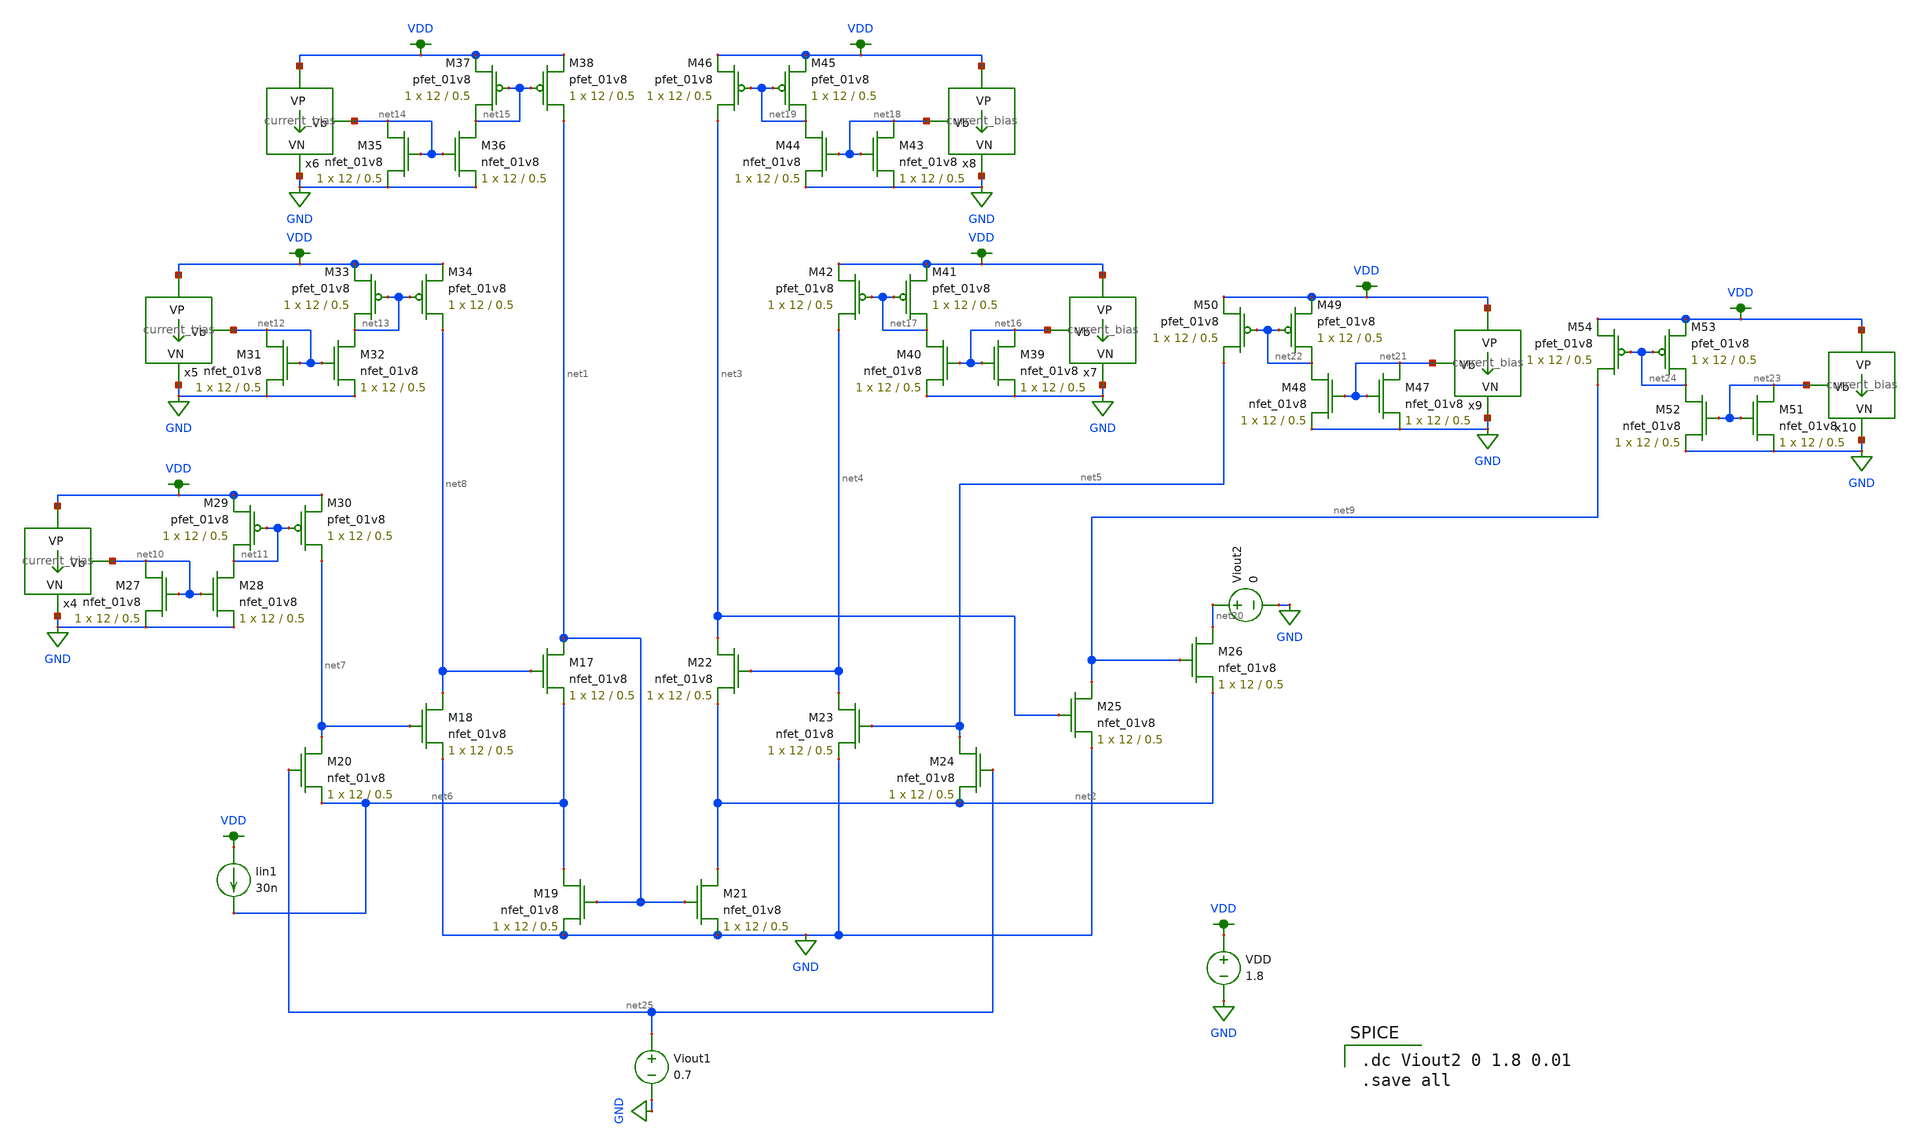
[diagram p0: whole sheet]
** sch_path: schematics/current mirrors/FVF_current_mirror_4.sch
**.subckt FVF_current_mirror_4
VDD VDD GND 1.8
XM19 net6 net1 GND GND sky130_fd_pr__nfet_01v8 L=0.5 W=12 nf=1 ad='int((nf+1)/2) * W/nf * 0.29' as='int((nf+2)/2) * W/nf * 0.29'
+ pd='2*int((nf+1)/2) * (W/nf + 0.29)' ps='2*int((nf+2)/2) * (W/nf + 0.29)' nrd='0.29 / W' nrs='0.29 / W'
+ sa=0 sb=0 sd=0 mult=1 m=1
XM21 net2 net1 GND GND sky130_fd_pr__nfet_01v8 L=0.5 W=12 nf=1 ad='int((nf+1)/2) * W/nf * 0.29' as='int((nf+2)/2) * W/nf * 0.29'
+ pd='2*int((nf+1)/2) * (W/nf + 0.29)' ps='2*int((nf+2)/2) * (W/nf + 0.29)' nrd='0.29 / W' nrs='0.29 / W'
+ sa=0 sb=0 sd=0 mult=1 m=1
XM22 net3 net4 net2 GND sky130_fd_pr__nfet_01v8 L=0.5 W=12 nf=1 ad='int((nf+1)/2) * W/nf * 0.29' as='int((nf+2)/2) * W/nf * 0.29'
+ pd='2*int((nf+1)/2) * (W/nf + 0.29)' ps='2*int((nf+2)/2) * (W/nf + 0.29)' nrd='0.29 / W' nrs='0.29 / W'
+ sa=0 sb=0 sd=0 mult=1 m=1
XM23 net4 net5 GND GND sky130_fd_pr__nfet_01v8 L=0.5 W=12 nf=1 ad='int((nf+1)/2) * W/nf * 0.29' as='int((nf+2)/2) * W/nf * 0.29'
+ pd='2*int((nf+1)/2) * (W/nf + 0.29)' ps='2*int((nf+2)/2) * (W/nf + 0.29)' nrd='0.29 / W' nrs='0.29 / W'
+ sa=0 sb=0 sd=0 mult=1 m=1
XM24 net5 net25 net2 GND sky130_fd_pr__nfet_01v8 L=0.5 W=12 nf=1 ad='int((nf+1)/2) * W/nf * 0.29' as='int((nf+2)/2) * W/nf * 0.29'
+ pd='2*int((nf+1)/2) * (W/nf + 0.29)' ps='2*int((nf+2)/2) * (W/nf + 0.29)' nrd='0.29 / W' nrs='0.29 / W'
+ sa=0 sb=0 sd=0 mult=1 m=1
XM17 net1 net8 net6 GND sky130_fd_pr__nfet_01v8 L=0.5 W=12 nf=1 ad='int((nf+1)/2) * W/nf * 0.29' as='int((nf+2)/2) * W/nf * 0.29'
+ pd='2*int((nf+1)/2) * (W/nf + 0.29)' ps='2*int((nf+2)/2) * (W/nf + 0.29)' nrd='0.29 / W' nrs='0.29 / W'
+ sa=0 sb=0 sd=0 mult=1 m=1
XM18 net8 net7 GND GND sky130_fd_pr__nfet_01v8 L=0.5 W=12 nf=1 ad='int((nf+1)/2) * W/nf * 0.29' as='int((nf+2)/2) * W/nf * 0.29'
+ pd='2*int((nf+1)/2) * (W/nf + 0.29)' ps='2*int((nf+2)/2) * (W/nf + 0.29)' nrd='0.29 / W' nrs='0.29 / W'
+ sa=0 sb=0 sd=0 mult=1 m=1
XM20 net7 net25 net6 GND sky130_fd_pr__nfet_01v8 L=0.5 W=12 nf=1 ad='int((nf+1)/2) * W/nf * 0.29' as='int((nf+2)/2) * W/nf * 0.29'
+ pd='2*int((nf+1)/2) * (W/nf + 0.29)' ps='2*int((nf+2)/2) * (W/nf + 0.29)' nrd='0.29 / W' nrs='0.29 / W'
+ sa=0 sb=0 sd=0 mult=1 m=1
XM25 net9 net3 GND GND sky130_fd_pr__nfet_01v8 L=0.5 W=12 nf=1 ad='int((nf+1)/2) * W/nf * 0.29' as='int((nf+2)/2) * W/nf * 0.29'
+ pd='2*int((nf+1)/2) * (W/nf + 0.29)' ps='2*int((nf+2)/2) * (W/nf + 0.29)' nrd='0.29 / W' nrs='0.29 / W'
+ sa=0 sb=0 sd=0 mult=1 m=1
XM26 net20 net9 net2 GND sky130_fd_pr__nfet_01v8 L=0.5 W=12 nf=1 ad='int((nf+1)/2) * W/nf * 0.29' as='int((nf+2)/2) * W/nf * 0.29'
+ pd='2*int((nf+1)/2) * (W/nf + 0.29)' ps='2*int((nf+2)/2) * (W/nf + 0.29)' nrd='0.29 / W' nrs='0.29 / W'
+ sa=0 sb=0 sd=0 mult=1 m=1
Iin1 VDD net6 30n
x4 VDD net10 GND current_bias
XM27 net10 net10 GND GND sky130_fd_pr__nfet_01v8 L=0.5 W=12 nf=1 ad='int((nf+1)/2) * W/nf * 0.29' as='int((nf+2)/2) * W/nf * 0.29'
+ pd='2*int((nf+1)/2) * (W/nf + 0.29)' ps='2*int((nf+2)/2) * (W/nf + 0.29)' nrd='0.29 / W' nrs='0.29 / W'
+ sa=0 sb=0 sd=0 mult=1 m=1
XM28 net11 net10 GND GND sky130_fd_pr__nfet_01v8 L=0.5 W=12 nf=1 ad='int((nf+1)/2) * W/nf * 0.29' as='int((nf+2)/2) * W/nf * 0.29'
+ pd='2*int((nf+1)/2) * (W/nf + 0.29)' ps='2*int((nf+2)/2) * (W/nf + 0.29)' nrd='0.29 / W' nrs='0.29 / W'
+ sa=0 sb=0 sd=0 mult=1 m=1
XM29 net11 net11 VDD VDD sky130_fd_pr__pfet_01v8 L=0.5 W=12 nf=1 ad='int((nf+1)/2) * W/nf * 0.29' as='int((nf+2)/2) * W/nf * 0.29'
+ pd='2*int((nf+1)/2) * (W/nf + 0.29)' ps='2*int((nf+2)/2) * (W/nf + 0.29)' nrd='0.29 / W' nrs='0.29 / W'
+ sa=0 sb=0 sd=0 mult=1 m=1
XM30 net7 net11 VDD VDD sky130_fd_pr__pfet_01v8 L=0.5 W=12 nf=1 ad='int((nf+1)/2) * W/nf * 0.29' as='int((nf+2)/2) * W/nf * 0.29'
+ pd='2*int((nf+1)/2) * (W/nf + 0.29)' ps='2*int((nf+2)/2) * (W/nf + 0.29)' nrd='0.29 / W' nrs='0.29 / W'
+ sa=0 sb=0 sd=0 mult=1 m=1
x5 VDD net12 GND current_bias
XM31 net12 net12 GND GND sky130_fd_pr__nfet_01v8 L=0.5 W=12 nf=1 ad='int((nf+1)/2) * W/nf * 0.29' as='int((nf+2)/2) * W/nf * 0.29'
+ pd='2*int((nf+1)/2) * (W/nf + 0.29)' ps='2*int((nf+2)/2) * (W/nf + 0.29)' nrd='0.29 / W' nrs='0.29 / W'
+ sa=0 sb=0 sd=0 mult=1 m=1
XM32 net13 net12 GND GND sky130_fd_pr__nfet_01v8 L=0.5 W=12 nf=1 ad='int((nf+1)/2) * W/nf * 0.29' as='int((nf+2)/2) * W/nf * 0.29'
+ pd='2*int((nf+1)/2) * (W/nf + 0.29)' ps='2*int((nf+2)/2) * (W/nf + 0.29)' nrd='0.29 / W' nrs='0.29 / W'
+ sa=0 sb=0 sd=0 mult=1 m=1
XM33 net13 net13 VDD VDD sky130_fd_pr__pfet_01v8 L=0.5 W=12 nf=1 ad='int((nf+1)/2) * W/nf * 0.29' as='int((nf+2)/2) * W/nf * 0.29'
+ pd='2*int((nf+1)/2) * (W/nf + 0.29)' ps='2*int((nf+2)/2) * (W/nf + 0.29)' nrd='0.29 / W' nrs='0.29 / W'
+ sa=0 sb=0 sd=0 mult=1 m=1
XM34 net8 net13 VDD VDD sky130_fd_pr__pfet_01v8 L=0.5 W=12 nf=1 ad='int((nf+1)/2) * W/nf * 0.29' as='int((nf+2)/2) * W/nf * 0.29'
+ pd='2*int((nf+1)/2) * (W/nf + 0.29)' ps='2*int((nf+2)/2) * (W/nf + 0.29)' nrd='0.29 / W' nrs='0.29 / W'
+ sa=0 sb=0 sd=0 mult=1 m=1
x6 VDD net14 GND current_bias
XM35 net14 net14 GND GND sky130_fd_pr__nfet_01v8 L=0.5 W=12 nf=1 ad='int((nf+1)/2) * W/nf * 0.29' as='int((nf+2)/2) * W/nf * 0.29'
+ pd='2*int((nf+1)/2) * (W/nf + 0.29)' ps='2*int((nf+2)/2) * (W/nf + 0.29)' nrd='0.29 / W' nrs='0.29 / W'
+ sa=0 sb=0 sd=0 mult=1 m=1
XM36 net15 net14 GND GND sky130_fd_pr__nfet_01v8 L=0.5 W=12 nf=1 ad='int((nf+1)/2) * W/nf * 0.29' as='int((nf+2)/2) * W/nf * 0.29'
+ pd='2*int((nf+1)/2) * (W/nf + 0.29)' ps='2*int((nf+2)/2) * (W/nf + 0.29)' nrd='0.29 / W' nrs='0.29 / W'
+ sa=0 sb=0 sd=0 mult=1 m=1
XM37 net15 net15 VDD VDD sky130_fd_pr__pfet_01v8 L=0.5 W=12 nf=1 ad='int((nf+1)/2) * W/nf * 0.29' as='int((nf+2)/2) * W/nf * 0.29'
+ pd='2*int((nf+1)/2) * (W/nf + 0.29)' ps='2*int((nf+2)/2) * (W/nf + 0.29)' nrd='0.29 / W' nrs='0.29 / W'
+ sa=0 sb=0 sd=0 mult=1 m=1
XM38 net1 net15 VDD VDD sky130_fd_pr__pfet_01v8 L=0.5 W=12 nf=1 ad='int((nf+1)/2) * W/nf * 0.29' as='int((nf+2)/2) * W/nf * 0.29'
+ pd='2*int((nf+1)/2) * (W/nf + 0.29)' ps='2*int((nf+2)/2) * (W/nf + 0.29)' nrd='0.29 / W' nrs='0.29 / W'
+ sa=0 sb=0 sd=0 mult=1 m=1
x7 VDD net16 GND current_bias
XM39 net16 net16 GND GND sky130_fd_pr__nfet_01v8 L=0.5 W=12 nf=1 ad='int((nf+1)/2) * W/nf * 0.29' as='int((nf+2)/2) * W/nf * 0.29'
+ pd='2*int((nf+1)/2) * (W/nf + 0.29)' ps='2*int((nf+2)/2) * (W/nf + 0.29)' nrd='0.29 / W' nrs='0.29 / W'
+ sa=0 sb=0 sd=0 mult=1 m=1
XM40 net17 net16 GND GND sky130_fd_pr__nfet_01v8 L=0.5 W=12 nf=1 ad='int((nf+1)/2) * W/nf * 0.29' as='int((nf+2)/2) * W/nf * 0.29'
+ pd='2*int((nf+1)/2) * (W/nf + 0.29)' ps='2*int((nf+2)/2) * (W/nf + 0.29)' nrd='0.29 / W' nrs='0.29 / W'
+ sa=0 sb=0 sd=0 mult=1 m=1
XM41 net17 net17 VDD VDD sky130_fd_pr__pfet_01v8 L=0.5 W=12 nf=1 ad='int((nf+1)/2) * W/nf * 0.29' as='int((nf+2)/2) * W/nf * 0.29'
+ pd='2*int((nf+1)/2) * (W/nf + 0.29)' ps='2*int((nf+2)/2) * (W/nf + 0.29)' nrd='0.29 / W' nrs='0.29 / W'
+ sa=0 sb=0 sd=0 mult=1 m=1
XM42 net4 net17 VDD VDD sky130_fd_pr__pfet_01v8 L=0.5 W=12 nf=1 ad='int((nf+1)/2) * W/nf * 0.29' as='int((nf+2)/2) * W/nf * 0.29'
+ pd='2*int((nf+1)/2) * (W/nf + 0.29)' ps='2*int((nf+2)/2) * (W/nf + 0.29)' nrd='0.29 / W' nrs='0.29 / W'
+ sa=0 sb=0 sd=0 mult=1 m=1
x8 VDD net18 GND current_bias
XM43 net18 net18 GND GND sky130_fd_pr__nfet_01v8 L=0.5 W=12 nf=1 ad='int((nf+1)/2) * W/nf * 0.29' as='int((nf+2)/2) * W/nf * 0.29'
+ pd='2*int((nf+1)/2) * (W/nf + 0.29)' ps='2*int((nf+2)/2) * (W/nf + 0.29)' nrd='0.29 / W' nrs='0.29 / W'
+ sa=0 sb=0 sd=0 mult=1 m=1
XM44 net19 net18 GND GND sky130_fd_pr__nfet_01v8 L=0.5 W=12 nf=1 ad='int((nf+1)/2) * W/nf * 0.29' as='int((nf+2)/2) * W/nf * 0.29'
+ pd='2*int((nf+1)/2) * (W/nf + 0.29)' ps='2*int((nf+2)/2) * (W/nf + 0.29)' nrd='0.29 / W' nrs='0.29 / W'
+ sa=0 sb=0 sd=0 mult=1 m=1
XM45 net19 net19 VDD VDD sky130_fd_pr__pfet_01v8 L=0.5 W=12 nf=1 ad='int((nf+1)/2) * W/nf * 0.29' as='int((nf+2)/2) * W/nf * 0.29'
+ pd='2*int((nf+1)/2) * (W/nf + 0.29)' ps='2*int((nf+2)/2) * (W/nf + 0.29)' nrd='0.29 / W' nrs='0.29 / W'
+ sa=0 sb=0 sd=0 mult=1 m=1
XM46 net3 net19 VDD VDD sky130_fd_pr__pfet_01v8 L=0.5 W=12 nf=1 ad='int((nf+1)/2) * W/nf * 0.29' as='int((nf+2)/2) * W/nf * 0.29'
+ pd='2*int((nf+1)/2) * (W/nf + 0.29)' ps='2*int((nf+2)/2) * (W/nf + 0.29)' nrd='0.29 / W' nrs='0.29 / W'
+ sa=0 sb=0 sd=0 mult=1 m=1
Viout2 net20 GND 0
x9 VDD net21 GND current_bias
XM47 net21 net21 GND GND sky130_fd_pr__nfet_01v8 L=0.5 W=12 nf=1 ad='int((nf+1)/2) * W/nf * 0.29' as='int((nf+2)/2) * W/nf * 0.29'
+ pd='2*int((nf+1)/2) * (W/nf + 0.29)' ps='2*int((nf+2)/2) * (W/nf + 0.29)' nrd='0.29 / W' nrs='0.29 / W'
+ sa=0 sb=0 sd=0 mult=1 m=1
XM48 net22 net21 GND GND sky130_fd_pr__nfet_01v8 L=0.5 W=12 nf=1 ad='int((nf+1)/2) * W/nf * 0.29' as='int((nf+2)/2) * W/nf * 0.29'
+ pd='2*int((nf+1)/2) * (W/nf + 0.29)' ps='2*int((nf+2)/2) * (W/nf + 0.29)' nrd='0.29 / W' nrs='0.29 / W'
+ sa=0 sb=0 sd=0 mult=1 m=1
XM49 net22 net22 VDD VDD sky130_fd_pr__pfet_01v8 L=0.5 W=12 nf=1 ad='int((nf+1)/2) * W/nf * 0.29' as='int((nf+2)/2) * W/nf * 0.29'
+ pd='2*int((nf+1)/2) * (W/nf + 0.29)' ps='2*int((nf+2)/2) * (W/nf + 0.29)' nrd='0.29 / W' nrs='0.29 / W'
+ sa=0 sb=0 sd=0 mult=1 m=1
XM50 net5 net22 VDD VDD sky130_fd_pr__pfet_01v8 L=0.5 W=12 nf=1 ad='int((nf+1)/2) * W/nf * 0.29' as='int((nf+2)/2) * W/nf * 0.29'
+ pd='2*int((nf+1)/2) * (W/nf + 0.29)' ps='2*int((nf+2)/2) * (W/nf + 0.29)' nrd='0.29 / W' nrs='0.29 / W'
+ sa=0 sb=0 sd=0 mult=1 m=1
x10 VDD net23 GND current_bias
XM51 net23 net23 GND GND sky130_fd_pr__nfet_01v8 L=0.5 W=12 nf=1 ad='int((nf+1)/2) * W/nf * 0.29' as='int((nf+2)/2) * W/nf * 0.29'
+ pd='2*int((nf+1)/2) * (W/nf + 0.29)' ps='2*int((nf+2)/2) * (W/nf + 0.29)' nrd='0.29 / W' nrs='0.29 / W'
+ sa=0 sb=0 sd=0 mult=1 m=1
XM52 net24 net23 GND GND sky130_fd_pr__nfet_01v8 L=0.5 W=12 nf=1 ad='int((nf+1)/2) * W/nf * 0.29' as='int((nf+2)/2) * W/nf * 0.29'
+ pd='2*int((nf+1)/2) * (W/nf + 0.29)' ps='2*int((nf+2)/2) * (W/nf + 0.29)' nrd='0.29 / W' nrs='0.29 / W'
+ sa=0 sb=0 sd=0 mult=1 m=1
XM53 net24 net24 VDD VDD sky130_fd_pr__pfet_01v8 L=0.5 W=12 nf=1 ad='int((nf+1)/2) * W/nf * 0.29' as='int((nf+2)/2) * W/nf * 0.29'
+ pd='2*int((nf+1)/2) * (W/nf + 0.29)' ps='2*int((nf+2)/2) * (W/nf + 0.29)' nrd='0.29 / W' nrs='0.29 / W'
+ sa=0 sb=0 sd=0 mult=1 m=1
XM54 net9 net24 VDD VDD sky130_fd_pr__pfet_01v8 L=0.5 W=12 nf=1 ad='int((nf+1)/2) * W/nf * 0.29' as='int((nf+2)/2) * W/nf * 0.29'
+ pd='2*int((nf+1)/2) * (W/nf + 0.29)' ps='2*int((nf+2)/2) * (W/nf + 0.29)' nrd='0.29 / W' nrs='0.29 / W'
+ sa=0 sb=0 sd=0 mult=1 m=1
Viout1 net25 GND 0.7
**** begin user architecture code

.option wnflag=1
.param MC_SWITCH=0.0
.lib ~/skywater/skywater-pdk/libraries/sky130_fd_pr_ngspice/latest/models/sky130.lib.spice tt


.dc Viout2 0 1.8 0.01
.save all

**** end user architecture code
**.ends
.GLOBAL VDD
.GLOBAL GND
.end
